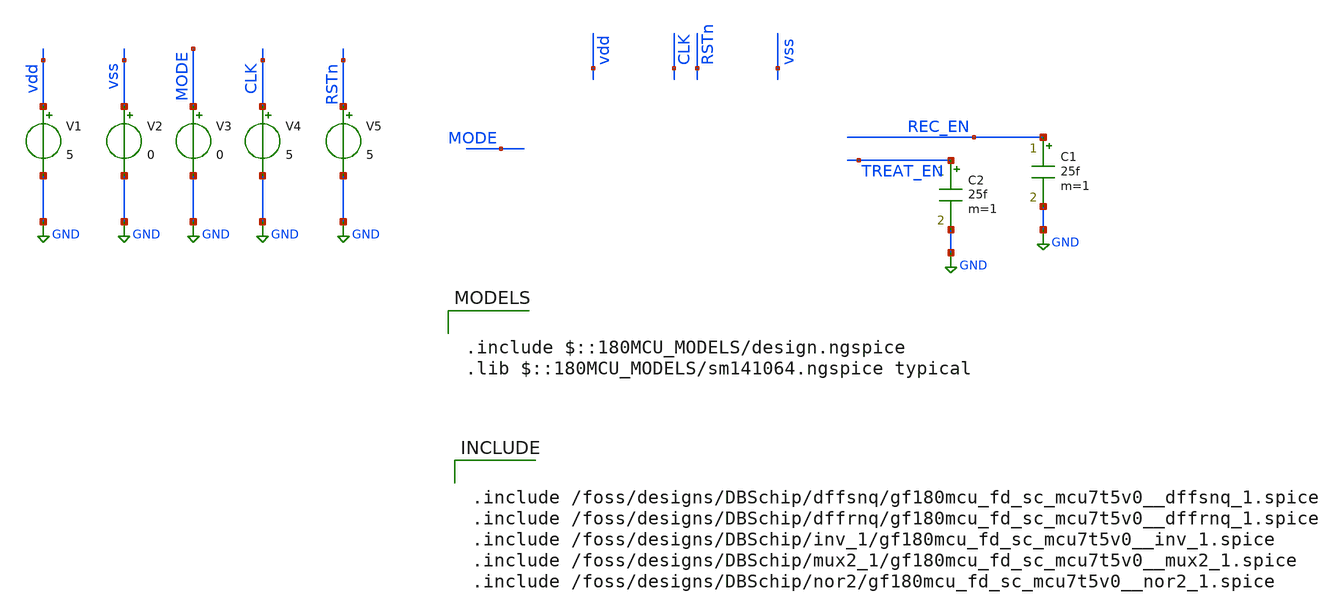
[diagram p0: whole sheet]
** sch_path: FSM/FSM_tb_postPEX.sch
**.subckt FSM_tb_postPEX
V1 vdd GND 5
V2 vss GND 0
V3 MODE GND 0
V4 CLK GND 5
V5 RSTn GND 5
C1 REC_EN GND 25f m=1
C2 TREAT_EN GND 25f m=1
**** begin user architecture code

.include $::180MCU_MODELS/design.ngspice
.lib $::180MCU_MODELS/sm141064.ngspice typical



.include /foss/designs/DBSchip/dffsnq/gf180mcu_fd_sc_mcu7t5v0__dffsnq_1.spice
.include /foss/designs/DBSchip/dffrnq/gf180mcu_fd_sc_mcu7t5v0__dffrnq_1.spice
.include /foss/designs/DBSchip/inv_1/gf180mcu_fd_sc_mcu7t5v0__inv_1.spice
.include /foss/designs/DBSchip/mux2_1/gf180mcu_fd_sc_mcu7t5v0__mux2_1.spice
.include /foss/designs/DBSchip/nor2/gf180mcu_fd_sc_mcu7t5v0__nor2_1.spice




* NGSPICE file created from FSM.ext - technology: gf180mcuD

.subckt dffsnq VNW VPW a_4883_3360# a_4479_2960# a_4470_3360# a_3430_3356# a_3430_2943#
+  a_6267_3356# a_4226_2960# a_6315_3300# a_5411_3360# a_4022_2960# a_4979_3257# a_4539_3312#  a_3902_3312#
+ a_5635_3360# a_3634_2943# a_3222_3356# a_3310_3312# a_7051_2873#
X0 a_7051_2873# a_6315_3300# a_3430_3356# VPW nfet_05v0 ad=0.3586p pd=2.51u as=0.3586p ps=2.51u
+ w=0.815u l=0.6u
X1 a_3634_2943# a_3222_3356# a_3430_3356# VPW nfet_05v0 ad=0.1782p pd=1.69u as=0.1053p ps=0.925u
+ w=0.405u l=0.6u
X2 a_3430_2943# a_3310_3312# a_3222_3356# VNW pfet_05v0 ad=0.2249p pd=1.385u as=0.3806p ps=2.61u
+ w=0.865u l=0.5u
X3 a_3430_3356# a_3310_3312# a_3222_3356# VPW nfet_05v0 ad=0.1053p pd=0.925u as=0.1782p ps=1.69u
+ w=0.405u l=0.6u
X4 a_4022_2960# a_3902_3312# a_3430_3356# VPW nfet_05v0 ad=93.59999f pd=0.88u as=0.1584p ps=1.6u
+ w=0.36u l=0.6u
X5 a_4539_3312# a_4979_3257# a_4883_3360# VPW nfet_05v0 ad=0.1989p pd=1.465u as=86.39999f ps=0.84u
+ w=0.36u l=0.6u
X6 a_5411_3360# a_3634_2943# a_4539_3312# VPW nfet_05v0 ad=93.59999f pd=0.88u as=0.1989p ps=1.465u
+ w=0.36u l=0.6u
X7 a_5635_3360# a_3634_2943# a_5411_3360# VNW pfet_05v0 ad=0.1826p pd=1.71u as=0.1079p ps=0.935u
+ w=0.415u l=0.5u
X8 a_5635_3360# a_4979_3257# a_3430_2943# VNW pfet_05v0 ad=0.2028p pd=1.3u as=0.3432p ps=2.44u
+ w=0.78u l=0.5u
X9 a_3430_3356# a_4539_3312# a_4470_3360# VPW nfet_05v0 ad=93.59999f pd=0.88u as=62.1f ps=0.705u
+ w=0.36u l=0.6u
X10 a_4226_2960# a_3222_3356# a_4022_2960# VPW nfet_05v0 ad=93.59999f pd=0.88u as=93.59999f ps=0.88u
+ w=0.36u l=0.6u
X11 a_3430_2943# a_4979_3257# a_4539_3312# VNW pfet_05v0 ad=0.4149p pd=2.65u as=0.1521p ps=1.105u
+ w=0.585u l=0.5u
X12 a_4883_3360# a_4226_2960# a_3430_3356# VPW nfet_05v0 ad=86.39999f pd=0.84u as=93.59999f ps=0.88u
+ w=0.36u l=0.6u
X13 a_6315_3300# a_5411_3360# a_3430_2943# VNW pfet_05v0 ad=0.3432p pd=2.44u as=0.3276p ps=1.62u
+ w=0.78u l=0.5u
X14 a_4470_3360# a_3634_2943# a_4226_2960# VPW nfet_05v0 ad=62.1f pd=0.705u as=93.59999f ps=0.88u
+ w=0.36u l=0.6u
X15 a_6315_3300# a_5411_3360# a_3430_3356# VPW nfet_05v0 ad=0.1782p pd=1.69u as=0.14985p ps=1.145u
+ w=0.405u l=0.6u
X16 a_3634_2943# a_3222_3356# a_3430_2943# VNW pfet_05v0 ad=0.3806p pd=2.61u as=0.2249p ps=1.385u
+ w=0.865u l=0.5u
X17 a_5411_3360# a_3222_3356# a_4539_3312# VNW pfet_05v0 ad=0.1079p pd=0.935u as=0.27805p ps=2.17u
+ w=0.415u l=0.5u
X18 a_3430_3356# a_6315_3300# a_6267_3356# VPW nfet_05v0 ad=0.14985p pd=1.145u as=48.6f ps=0.645u
+ w=0.405u l=0.6u
X19 a_4226_2960# a_3634_2943# a_4022_2960# VNW pfet_05v0 ad=0.19315p pd=1.27u as=0.1313p ps=1.025u
+ w=0.505u l=0.5u
X20 a_4539_3312# a_4226_2960# a_3430_2943# VNW pfet_05v0 ad=0.1521p pd=1.105u as=0.3975p ps=2.185u
+ w=0.585u l=0.5u
X21 a_6267_3356# a_4979_3257# a_5635_3360# VPW nfet_05v0 ad=48.6f pd=0.645u as=0.3123p ps=2.38u
+ w=0.405u l=0.6u
X22 a_4022_2960# a_3902_3312# a_3430_2943# VNW pfet_05v0 ad=0.1313p pd=1.025u as=0.22725p ps=1.91u
+ w=0.505u l=0.5u
X23 a_3430_2943# a_6315_3300# a_5635_3360# VNW pfet_05v0 ad=0.3276p pd=1.62u as=0.2028p ps=1.3u
+ w=0.78u l=0.5u
X24 a_4479_2960# a_3222_3356# a_4226_2960# VNW pfet_05v0 ad=0.101p pd=0.905u as=0.19315p ps=1.27u
+ w=0.505u l=0.5u
X25 a_5635_3360# a_3222_3356# a_5411_3360# VPW nfet_05v0 ad=0.2898p pd=2.33u as=93.59999f ps=0.88u
+ w=0.36u l=0.6u
X26 a_7051_2873# a_6315_3300# a_3430_2943# VNW pfet_05v0 ad=0.6561p pd=3.51u as=0.5346p ps=3.31u
+ w=1.215u l=0.5u
X27 a_3430_2943# a_4539_3312# a_4479_2960# VNW pfet_05v0 ad=0.3975p pd=2.185u as=0.101p ps=0.905u
+ w=0.505u l=0.5u
C0 a_4979_3257# a_3222_3356# 0.07762f
C1 a_5411_3360# a_6267_3356# 0.00413f
C2 a_5411_3360# a_3430_2943# 0.07341f
C3 a_4226_2960# a_4479_2960# 0.00215f
C4 a_4226_2960# a_4539_3312# 0.38667f
C5 VNW a_3310_3312# 0.13342f
C6 a_3430_2943# a_3902_3312# 0.00494f
C7 VNW a_3430_3356# 0.00946f
C8 a_4979_3257# a_4539_3312# 0.07298f
C9 a_4226_2960# a_4470_3360# 0
C10 a_3430_2943# a_7051_2873# 0.28218f
C11 a_5411_3360# a_6315_3300# 0.51404f
C12 a_3430_2943# a_6267_3356# 0
C13 a_3634_2943# a_3310_3312# 0.00131f
C14 a_5411_3360# a_4979_3257# 0.0706f
C15 a_3634_2943# a_3430_3356# 1.08287f
C16 a_4226_2960# a_3902_3312# 0
C17 a_3222_3356# a_3310_3312# 0.70196f
C18 a_3222_3356# a_3430_3356# 0.29459f
C19 a_7051_2873# a_6315_3300# 0.17947f
C20 a_5635_3360# VNW 0.04382f
C21 a_4022_2960# a_3430_3356# 0.05001f
C22 a_3430_2943# a_6315_3300# 0.35131f
C23 a_4539_3312# a_3430_3356# 0.02825f
C24 a_3634_2943# VNW 0.40096f
C25 a_3430_2943# a_4226_2960# 0.03968f
C26 VNW a_3222_3356# 0.90809f
C27 a_5635_3360# a_3634_2943# 0.05668f
C28 a_4979_3257# a_3430_2943# 0.12782f
C29 a_4470_3360# a_3430_3356# 0.00364f
C30 a_4022_2960# VNW 0.01368f
C31 a_5635_3360# a_3222_3356# 0.00597f
C32 a_5411_3360# a_3430_3356# 1.19047f
C33 VNW a_4539_3312# 0.21951f
C34 a_3634_2943# a_3222_3356# 0.47313f
C35 a_5635_3360# a_4539_3312# 0
C36 a_4022_2960# a_3634_2943# 0.42776f
C37 a_3902_3312# a_3430_3356# 0.06788f
C38 a_4979_3257# a_6315_3300# 0.08929f
C39 a_4979_3257# a_4226_2960# 0.06324f
C40 a_4022_2960# a_3222_3356# 0.0157f
C41 a_7051_2873# a_3430_3356# 0.13127f
C42 a_5411_3360# VNW 0.20903f
C43 a_3634_2943# a_4539_3312# 0.31725f
C44 a_3222_3356# a_4479_2960# 0.00838f
C45 a_5411_3360# a_5635_3360# 0.56917f
C46 a_4539_3312# a_3222_3356# 0.84088f
C47 a_3430_2943# a_3310_3312# 0.02223f
C48 a_3430_2943# a_3430_3356# 0.01381f
C49 a_3634_2943# a_4470_3360# 0.00269f
C50 VNW a_3902_3312# 0.16142f
C51 VNW a_7051_2873# 0.03162f
C52 a_4883_3360# a_3634_2943# 0.00762f
C53 a_4539_3312# a_4479_2960# 0
C54 a_5411_3360# a_3634_2943# 0.154f
C55 a_5411_3360# a_3222_3356# 0.15368f
C56 a_3430_3356# a_6315_3300# 0.13908f
C57 a_3430_2943# VNW 0.53642f
C58 a_3634_2943# a_3902_3312# 0.4001f
C59 a_4226_2960# a_3430_3356# 0.06133f
C60 a_5635_3360# a_6267_3356# 0.0012f
C61 a_3430_2943# a_5635_3360# 0.20863f
C62 a_3902_3312# a_3222_3356# 0.0927f
C63 a_3634_2943# a_7051_2873# 0
C64 a_4883_3360# a_4539_3312# 0.00275f
C65 a_4022_2960# a_3902_3312# 0.1081f
C66 a_4979_3257# a_3430_3356# 0.01045f
C67 a_7051_2873# a_3222_3356# 0
C68 a_5411_3360# a_4539_3312# 0.15287f
C69 a_3430_2943# a_3634_2943# 0.62458f
C70 VNW a_6315_3300# 0.32346f
C71 a_4226_2960# VNW 0.22464f
C72 a_3430_2943# a_3222_3356# 1.41458f
C73 a_5635_3360# a_6315_3300# 0.00955f
C74 a_4979_3257# VNW 0.81105f
C75 a_4979_3257# a_5635_3360# 0.30222f
C76 a_3430_2943# a_4539_3312# 0.01626f
C77 a_3634_2943# a_6315_3300# 0
C78 a_4226_2960# a_3634_2943# 0.86961f
C79 a_5411_3360# a_7051_2873# 0
C80 a_3222_3356# a_6315_3300# 0
C81 a_4226_2960# a_3222_3356# 0.20702f
C82 a_3310_3312# a_3430_3356# 0.02287f
C83 a_4979_3257# a_3634_2943# 0.0839f
C84 a_4226_2960# a_4022_2960# 0.06821f
C85 VNW VPW 6.37108f
C86 a_7051_2873# VPW 0.10557f
C87 a_6315_3300# VPW 0.58406f
C88 a_5635_3360# VPW 0.04999f
C89 a_5411_3360# VPW 0.43408f
C90 a_3430_2943# VPW 0.83584f
C91 a_4022_2960# VPW 0.01977f
C92 a_4979_3257# VPW 0.71025f
C93 a_4226_2960# VPW 0.30208f
C94 a_4539_3312# VPW 0.28651f
C95 a_3902_3312# VPW 0.24718f
C96 a_3634_2943# VPW 1.21246f
C97 a_3430_3356# VPW 1.53117f
C98 a_3310_3312# VPW 0.2938f
C99 a_3222_3356# VPW 1.31514f
.ends

.subckt mux21 VNW VPW a_n2035_3346# a_n2339_2762# a_n2427_3346# a_n2807_3163# a_n2394_2806#
+  a_n1987_2762# a_n2687_2806# a_n2687_3290# a_n2035_2806# a_n2547_3163# a_n2379_3163#  a_n2895_3290#
X0 a_n2035_2806# a_n2379_3163# a_n2807_3163# VNW pfet_05v0 ad=73.8f pd=0.855u as=0.1599p ps=1.135u
+ w=0.615u l=0.5u
X1 a_n2687_2806# a_n1987_2762# a_n2035_2806# VNW pfet_05v0 ad=0.1599p pd=1.135u as=73.8f ps=0.855u
+ w=0.615u l=0.5u
X2 a_n2687_3290# a_n1987_2762# a_n2035_3346# VPW nfet_05v0 ad=93.59999f pd=0.88u as=43.2f ps=0.6u
+ w=0.36u l=0.6u
X3 a_n2427_3346# a_n2547_3163# a_n2687_3290# VPW nfet_05v0 ad=43.2f pd=0.6u as=0.218p ps=1.52u
+ w=0.36u l=0.6u
X4 a_n2339_2762# a_n2379_3163# a_n2687_3290# VPW nfet_05v0 ad=0.1584p pd=1.6u as=93.59999f ps=0.88u
+ w=0.36u l=0.6u
X5 a_n2807_3163# a_n2339_2762# a_n2394_2806# VNW pfet_05v0 ad=0.1599p pd=1.135u as=84.55f ps=0.89u
+ w=0.615u l=0.5u
X6 a_n2687_2806# a_n2807_3163# a_n2895_3290# VNW pfet_05v0 ad=0.42982p pd=2.185u as=0.5368p ps=3.32u
+ w=1.22u l=0.5u
X7 a_n2807_3163# a_n2379_3163# a_n2427_3346# VPW nfet_05v0 ad=93.59999f pd=0.88u as=43.2f ps=0.6u
+ w=0.36u l=0.6u
X8 a_n2035_3346# a_n2339_2762# a_n2807_3163# VPW nfet_05v0 ad=43.2f pd=0.6u as=93.59999f ps=0.88u
+ w=0.36u l=0.6u
X9 a_n2339_2762# a_n2379_3163# a_n2687_2806# VNW pfet_05v0 ad=0.2706p pd=2.11u as=0.1599p ps=1.135u
+ w=0.615u l=0.5u
X10 a_n2687_3290# a_n2807_3163# a_n2895_3290# VPW nfet_05v0 ad=0.218p pd=1.52u as=0.3608p ps=2.52u
+ w=0.82u l=0.6u
X11 a_n2394_2806# a_n2547_3163# a_n2687_2806# VNW pfet_05v0 ad=84.55f pd=0.89u as=0.42982p ps=2.185u
+ w=0.615u l=0.5u
C0 a_n2379_3163# a_n2394_2806# 0
C1 a_n2339_2762# a_n1987_2762# 0.44871f
C2 a_n2339_2762# a_n2807_3163# 0.03132f
C3 a_n2547_3163# a_n2687_3290# 0.01931f
C4 a_n1987_2762# a_n2687_2806# 0.02643f
C5 VNW a_n2379_3163# 0.35854f
C6 a_n2807_3163# a_n2687_2806# 0.57837f
C7 a_n2547_3163# a_n2895_3290# 0.00111f
C8 a_n2807_3163# a_n1987_2762# 0.00457f
C9 a_n2547_3163# a_n2394_2806# 0
C10 a_n2339_2762# a_n2379_3163# 0.31909f
C11 a_n2035_2806# a_n2339_2762# 0
C12 a_n2687_3290# a_n2895_3290# 0.07969f
C13 a_n2687_2806# a_n2379_3163# 0.20342f
C14 a_n2035_2806# a_n2687_2806# 0.00486f
C15 a_n2547_3163# VNW 0.19864f
C16 a_n2035_3346# a_n2687_3290# 0.0022f
C17 a_n1987_2762# a_n2379_3163# 0.61564f
C18 a_n2687_3290# VNW 0.00651f
C19 a_n2807_3163# a_n2379_3163# 0.22045f
C20 a_n2035_2806# a_n2807_3163# 0.00106f
C21 a_n2339_2762# a_n2547_3163# 0.06637f
C22 a_n2807_3163# a_n2427_3346# 0.00317f
C23 a_n2687_2806# a_n2547_3163# 0.01544f
C24 VNW a_n2895_3290# 0.03019f
C25 a_n2339_2762# a_n2687_3290# 0.30506f
C26 a_n2687_2806# a_n2687_3290# 0.01065f
C27 a_n1987_2762# a_n2547_3163# 0
C28 a_n2035_2806# a_n2379_3163# 0.00276f
C29 a_n2807_3163# a_n2547_3163# 0.45783f
C30 a_n1987_2762# a_n2687_3290# 0.03158f
C31 a_n2339_2762# a_n2394_2806# 0
C32 a_n2807_3163# a_n2687_3290# 0.53787f
C33 a_n2687_2806# a_n2895_3290# 0.09438f
C34 a_n2035_3346# a_n2339_2762# 0.00166f
C35 a_n2687_2806# a_n2394_2806# 0.0019f
C36 a_n2339_2762# VNW 0.27449f
C37 a_n2547_3163# a_n2379_3163# 0.3671f
C38 a_n2807_3163# a_n2895_3290# 0.13298f
C39 a_n2687_2806# VNW 0.16121f
C40 a_n2807_3163# a_n2394_2806# 0.00556f
C41 a_n2427_3346# a_n2547_3163# 0
C42 a_n2035_3346# a_n2807_3163# 0.00101f
C43 a_n2687_3290# a_n2379_3163# 0.04663f
C44 a_n1987_2762# VNW 0.18121f
C45 a_n2427_3346# a_n2687_3290# 0
C46 a_n2807_3163# VNW 0.16283f
C47 a_n2339_2762# a_n2687_2806# 0.14217f
C48 VNW VPW 2.50194f
C49 a_n2687_2806# VPW 0.34621f
C50 a_n1987_2762# VPW 0.29252f
C51 a_n2339_2762# VPW 0.4399f
C52 a_n2379_3163# VPW 0.64969f
C53 a_n2547_3163# VPW 0.31807f
C54 a_n2687_3290# VPW 0.57909f
C55 a_n2895_3290# VPW 0.11309f
C56 a_n2807_3163# VPW 0.3249f
.ends

.subckt dffrnq VNW VPW a_1667_2471# a_563_2471# a_311_2787# a_395_2471# a_n649_2466#  a_2776_2384#
+ a_1772_2427# a_1355_2471# a_n649_2787# a_2148_2471# a_611_2339# a_n857_2466#  a_n197_2617# a_n445_2787#
+ a_415_2738# a_107_2787# a_n97_2787# a_n769_2422#
X0 a_n649_2787# a_n769_2422# a_n857_2466# VNW pfet_05v0 ad=0.2249p pd=1.385u as=0.3806p ps=2.61u
+ w=0.865u l=0.5u
X1 a_311_2787# a_n857_2466# a_107_2787# VNW pfet_05v0 ad=0.2028p pd=1.3u as=0.2028p ps=1.3u w=0.78u
+ l=0.5u
X2 a_2148_2471# a_611_2339# a_n649_2466# VPW nfet_05v0 ad=0.134p pd=1.1u as=0.1224p ps=1.04u w=0.36u
+ l=0.6u
X3 a_1355_2471# a_n445_2787# a_415_2738# VPW nfet_05v0 ad=0.2007p pd=1.475u as=0.2007p ps=1.475u
+ w=0.36u l=0.6u
X4 a_107_2787# a_n857_2466# a_n97_2787# VPW nfet_05v0 ad=93.59999f pd=0.88u as=93.59999f ps=0.88u
+ w=0.36u l=0.6u
X5 a_311_2787# a_611_2339# a_n649_2787# VNW pfet_05v0 ad=0.3432p pd=2.44u as=0.45p ps=2.02u w=0.78u
+ l=0.5u
X6 a_n649_2466# a_611_2339# a_563_2471# VPW nfet_05v0 ad=0.2016p pd=1.48u as=43.2f ps=0.6u w=0.36u
+ l=0.6u
X7 a_2776_2384# a_1772_2427# a_n649_2466# VPW nfet_05v0 ad=0.3586p pd=2.51u as=0.3586p ps=2.51u
+ w=0.815u l=0.6u
X8 a_n649_2787# a_1772_2427# a_1667_2471# VNW pfet_05v0 ad=0.29465p pd=1.74u as=0.1313p ps=1.025u
+ w=0.505u l=0.5u
X9 a_107_2787# a_n445_2787# a_n97_2787# VNW pfet_05v0 ad=0.2028p pd=1.3u as=0.2028p ps=1.3u w=0.78u
+ l=0.5u
X10 a_n97_2787# a_n197_2617# a_n649_2466# VPW nfet_05v0 ad=93.59999f pd=0.88u as=0.1584p ps=1.6u
+ w=0.36u l=0.6u
X11 a_563_2471# a_415_2738# a_395_2471# VPW nfet_05v0 ad=43.2f pd=0.6u as=43.2f ps=0.6u w=0.36u
+ l=0.6u
X12 a_n649_2787# a_1355_2471# a_1772_2427# VNW pfet_05v0 ad=0.44p pd=2.88u as=0.26p ps=1.52u w=1u
+ l=0.5u
X13 a_395_2471# a_n445_2787# a_107_2787# VPW nfet_05v0 ad=43.2f pd=0.6u as=93.59999f ps=0.88u
+ w=0.36u l=0.6u
X14 a_415_2738# a_107_2787# a_n649_2787# VNW pfet_05v0 ad=0.2424p pd=1.465u as=0.2222p ps=1.89u
+ w=0.505u l=0.5u
X15 a_2776_2384# a_1772_2427# a_n649_2787# VNW pfet_05v0 ad=0.5346p pd=3.31u as=0.5346p ps=3.31u
+ w=1.215u l=0.5u
X16 a_n649_2466# a_1772_2427# a_1667_2471# VPW nfet_05v0 ad=0.1224p pd=1.04u as=94.5f ps=0.885u
+ w=0.36u l=0.6u
X17 a_n97_2787# a_n197_2617# a_n649_2787# VNW pfet_05v0 ad=0.2028p pd=1.3u as=0.3432p ps=2.44u
+ w=0.78u l=0.5u
X18 a_n445_2787# a_n857_2466# a_n649_2787# VNW pfet_05v0 ad=0.3806p pd=2.61u as=0.2249p ps=1.385u
+ w=0.865u l=0.5u
X19 a_n649_2787# a_415_2738# a_311_2787# VNW pfet_05v0 ad=0.45p pd=2.02u as=0.2028p ps=1.3u w=0.78u
+ l=0.5u
X20 a_n649_2466# a_n769_2422# a_n857_2466# VPW nfet_05v0 ad=0.1053p pd=0.925u as=0.1782p ps=1.69u
+ w=0.405u l=0.6u
X21 a_1667_2471# a_n857_2466# a_1355_2471# VPW nfet_05v0 ad=94.5f pd=0.885u as=0.2007p ps=1.475u
+ w=0.36u l=0.6u
X22 a_415_2738# a_107_2787# a_n649_2466# VPW nfet_05v0 ad=0.2007p pd=1.475u as=0.2016p ps=1.48u
+ w=0.36u l=0.6u
X23 a_n445_2787# a_n857_2466# a_n649_2466# VPW nfet_05v0 ad=0.1782p pd=1.69u as=0.1053p ps=0.925u
+ w=0.405u l=0.6u
X24 a_1355_2471# a_n857_2466# a_415_2738# VNW pfet_05v0 ad=0.25375p pd=1.51u as=0.2424p ps=1.465u
+ w=0.505u l=0.5u
X25 a_1772_2427# a_1355_2471# a_2148_2471# VPW nfet_05v0 ad=0.176p pd=1.68u as=0.134p ps=1.1u w=0.4u
+ l=0.6u
X26 a_1667_2471# a_n445_2787# a_1355_2471# VNW pfet_05v0 ad=0.1313p pd=1.025u as=0.25375p ps=1.51u
+ w=0.505u l=0.5u
X27 a_1772_2427# a_611_2339# a_n649_2787# VNW pfet_05v0 ad=0.26p pd=1.52u as=0.29465p ps=1.74u w=1u
+ l=0.5u
C0 a_311_2787# a_n445_2787# 0.009f
C1 a_n197_2617# a_n445_2787# 0.32879f
C2 a_611_2339# a_n649_2787# 0.03498f
C3 a_n649_2787# a_1355_2471# 1.11667f
C4 VNW a_n649_2787# 0.50089f
C5 a_n649_2466# a_n649_2787# 0.01338f
C6 a_n857_2466# a_n445_2787# 0.53697f
C7 a_107_2787# a_n649_2787# 0.11921f
C8 a_n769_2422# a_n857_2466# 0.6696f
C9 a_611_2339# a_1355_2471# 0.09434f
C10 a_n197_2617# a_n97_2787# 0.08286f
C11 VNW a_611_2339# 0.32949f
C12 VNW a_1355_2471# 0.21243f
C13 a_n649_2466# a_611_2339# 0.44197f
C14 a_n649_2466# a_1355_2471# 0.03047f
C15 a_611_2339# a_107_2787# 0.0832f
C16 a_107_2787# a_1355_2471# 0.00123f
C17 VNW a_n649_2466# 0.0106f
C18 a_1772_2427# a_n857_2466# 0.01904f
C19 VNW a_107_2787# 0.24136f
C20 a_n649_2466# a_107_2787# 0.04356f
C21 a_1667_2471# a_n857_2466# 0.00367f
C22 a_n857_2466# a_n97_2787# 0.01185f
C23 a_n857_2466# a_2776_2384# 0
C24 a_n649_2466# a_563_2471# 0.0019f
C25 a_107_2787# a_563_2471# 0
C26 a_415_2738# a_n445_2787# 0.8821f
C27 a_n649_2466# a_395_2471# 0.0017f
C28 a_107_2787# a_395_2471# 0
C29 a_n649_2787# a_311_2787# 0.28263f
C30 a_n197_2617# a_n649_2787# 0.00937f
C31 a_611_2339# a_311_2787# 0.02104f
C32 a_n857_2466# a_n649_2787# 0.41709f
C33 VNW a_311_2787# 0.01627f
C34 VNW a_n197_2617# 0.12821f
C35 a_2148_2471# a_1772_2427# 0.00177f
C36 a_n649_2466# a_n197_2617# 0.06462f
C37 a_107_2787# a_311_2787# 0.66083f
C38 a_n197_2617# a_107_2787# 0
C39 a_611_2339# a_n857_2466# 0.0801f
C40 a_n857_2466# a_1355_2471# 0.0428f
C41 VNW a_n857_2466# 1.28735f
C42 a_n649_2466# a_n857_2466# 0.29126f
C43 a_107_2787# a_n857_2466# 0.08126f
C44 a_n769_2422# a_n445_2787# 0.00276f
C45 a_1772_2427# a_n445_2787# 0.02046f
C46 a_1667_2471# a_n445_2787# 0.27749f
C47 a_n97_2787# a_n445_2787# 0.40164f
C48 a_415_2738# a_n649_2787# 0.09419f
C49 a_1667_2471# a_1772_2427# 0.11606f
C50 a_415_2738# a_611_2339# 0.07929f
C51 a_415_2738# a_1355_2471# 0.05672f
C52 a_611_2339# a_2148_2471# 0.01068f
C53 VNW a_415_2738# 0.14901f
C54 a_1772_2427# a_2776_2384# 0.10944f
C55 a_n649_2466# a_415_2738# 0.01387f
C56 a_415_2738# a_107_2787# 0.93419f
C57 a_n857_2466# a_311_2787# 0.007f
C58 a_n197_2617# a_n857_2466# 0.09411f
C59 a_n649_2787# a_n445_2787# 0.45627f
C60 a_n769_2422# a_n649_2787# 0.02303f
C61 a_611_2339# a_n445_2787# 0.07873f
C62 a_n445_2787# a_1355_2471# 0.51037f
C63 VNW a_n445_2787# 0.34128f
C64 a_1772_2427# a_n649_2787# 0.10205f
C65 a_n649_2466# a_n445_2787# 1.20207f
C66 a_107_2787# a_n445_2787# 0.36196f
C67 a_1667_2471# a_n649_2787# 0.00217f
C68 a_n769_2422# VNW 0.1337f
C69 a_n649_2787# a_n97_2787# 0
C70 a_n769_2422# a_n649_2466# 0.02195f
C71 a_n649_2787# a_2776_2384# 0.14934f
C72 a_611_2339# a_1772_2427# 0.33647f
C73 a_1772_2427# a_1355_2471# 0.63332f
C74 a_415_2738# a_311_2787# 0.02667f
C75 a_563_2471# a_n445_2787# 0.00227f
C76 VNW a_1772_2427# 0.35472f
C77 a_1667_2471# a_611_2339# 0.03878f
C78 a_n649_2466# a_1772_2427# 0.185f
C79 a_1667_2471# a_1355_2471# 0.11969f
C80 VNW a_1667_2471# 0.02016f
C81 VNW a_n97_2787# 0.01023f
C82 a_n649_2466# a_1667_2471# 0.1285f
C83 a_611_2339# a_2776_2384# 0
C84 a_n649_2466# a_n97_2787# 0.05215f
C85 a_2776_2384# a_1355_2471# 0.01436f
C86 a_107_2787# a_n97_2787# 0.04844f
C87 VNW a_2776_2384# 0.03444f
C88 a_n649_2466# a_2776_2384# 0.1134f
C89 a_415_2738# a_n857_2466# 0.05539f
C90 a_395_2471# a_n445_2787# 0.00207f
C91 VNW VPW 6.06621f
C92 a_2776_2384# VPW 0.11476f
C93 a_n649_2466# VPW 1.26186f
C94 a_1667_2471# VPW 0.01697f
C95 a_1772_2427# VPW 0.62251f
C96 a_1355_2471# VPW 0.37166f
C97 a_611_2339# VPW 1.36673f
C98 a_311_2787# VPW 0.01297f
C99 a_107_2787# VPW 0.29173f
C100 a_n97_2787# VPW 0.02321f
C101 a_415_2738# VPW 0.27904f
C102 a_n197_2617# VPW 0.25343f
C103 a_n445_2787# VPW 0.68441f
C104 a_n649_2787# VPW 0.80211f
C105 a_n769_2422# VPW 0.29458f
C106 a_n857_2466# VPW 1.43686f
.ends

.subckt nor2_1 a_n5117_4170# a_n4805_3759# a_n5029_3759# a_n5117_3803# a_n4909_3803#  a_n4929_4170#
+ w_n5239_4050# VSUBS
X0 a_n5117_3803# a_n4805_3759# a_n4909_3803# VSUBS nfet_05v0 ad=0.2486p pd=2.01u as=0.1469p
+ ps=1.085u w=0.565u l=0.6u
X1 a_n4929_4170# a_n5029_3759# a_n5117_4170# w_n5239_4050# pfet_05v0 ad=0.4087p pd=1.89u as=0.5368p
+ ps=3.32u w=1.22u l=0.5u
X2 a_n4909_3803# a_n5029_3759# a_n5117_3803# VSUBS nfet_05v0 ad=0.1469p pd=1.085u as=0.2486p
+ ps=2.01u w=0.565u l=0.6u
X3 a_n4909_3803# a_n4805_3759# a_n4929_4170# w_n5239_4050# pfet_05v0 ad=0.5368p pd=3.32u as=0.4087p
+ ps=1.89u w=1.22u l=0.5u
C0 a_n5029_3759# a_n4805_3759# 0.03781f
C1 a_n5117_3803# w_n5239_4050# 0.01397f
C2 w_n5239_4050# a_n4805_3759# 0.12879f
C3 a_n4909_3803# a_n5029_3759# 0.37841f
C4 a_n4909_3803# w_n5239_4050# 0.0217f
C5 a_n5029_3759# w_n5239_4050# 0.1288f
C6 a_n4929_4170# a_n5117_4170# 0.01396f
C7 a_n5117_3803# a_n5117_4170# 0.02578f
C8 a_n5117_4170# a_n4805_3759# 0.02269f
C9 a_n4929_4170# a_n5117_3803# 0
C10 a_n4909_3803# a_n5117_4170# 0.11792f
C11 a_n5117_3803# a_n4805_3759# 0.13941f
C12 a_n5117_4170# a_n5029_3759# 0.25532f
C13 a_n5117_4170# w_n5239_4050# 0.09389f
C14 a_n4909_3803# a_n4929_4170# 0.02369f
C15 a_n4909_3803# a_n5117_3803# 0.10123f
C16 a_n4909_3803# a_n4805_3759# 0.46284f
C17 a_n4929_4170# a_n5029_3759# 0.00898f
C18 a_n5117_3803# a_n5029_3759# 0.04335f
C19 a_n5117_3803# VSUBS 0.33074f
C20 a_n4909_3803# VSUBS 0.06183f
C21 a_n5117_4170# VSUBS 0.21851f
C22 a_n4805_3759# VSUBS 0.32338f
C23 a_n5029_3759# VSUBS 0.33451f
C24 w_n5239_4050# VSUBS 1.31158f
.ends

.subckt nor2_2 a_n3913_1897# a_n3601_1486# a_n3705_1530# a_n3725_1897# a_n3825_1486#  w_n4035_1777#
+ a_n3913_1530# VSUBS
X0 a_n3725_1897# a_n3825_1486# a_n3913_1897# w_n4035_1777# pfet_05v0 ad=0.4087p pd=1.89u as=0.5368p
+ ps=3.32u w=1.22u l=0.5u
X1 a_n3705_1530# a_n3825_1486# a_n3913_1530# VSUBS nfet_05v0 ad=0.1469p pd=1.085u as=0.2486p
+ ps=2.01u w=0.565u l=0.6u
X2 a_n3913_1530# a_n3601_1486# a_n3705_1530# VSUBS nfet_05v0 ad=0.2486p pd=2.01u as=0.1469p
+ ps=1.085u w=0.565u l=0.6u
X3 a_n3705_1530# a_n3601_1486# a_n3725_1897# w_n4035_1777# pfet_05v0 ad=0.5368p pd=3.32u as=0.4087p
+ ps=1.89u w=1.22u l=0.5u
C0 a_n3705_1530# a_n3601_1486# 0.57973f
C1 w_n4035_1777# a_n3705_1530# 0.01867f
C2 a_n3725_1897# a_n3825_1486# 0.00898f
C3 a_n3913_1530# a_n3705_1530# 0.08687f
C4 a_n3913_1897# a_n3705_1530# 0.11792f
C5 a_n3825_1486# a_n3705_1530# 0.37841f
C6 a_n3725_1897# a_n3705_1530# 0.02369f
C7 w_n4035_1777# a_n3601_1486# 0.13462f
C8 a_n3913_1530# a_n3601_1486# 0.16863f
C9 a_n3913_1897# a_n3601_1486# 0.02804f
C10 w_n4035_1777# a_n3913_1530# 0.01057f
C11 w_n4035_1777# a_n3913_1897# 0.09154f
C12 a_n3913_1530# a_n3913_1897# 0.02322f
C13 a_n3825_1486# a_n3601_1486# 0.03781f
C14 w_n4035_1777# a_n3825_1486# 0.1288f
C15 a_n3913_1530# a_n3825_1486# 0.04335f
C16 a_n3825_1486# a_n3913_1897# 0.25532f
C17 a_n3913_1530# a_n3725_1897# 0
C18 a_n3725_1897# a_n3913_1897# 0.01396f
C19 a_n3913_1530# VSUBS 0.33149f
C20 a_n3705_1530# VSUBS 0.06f
C21 a_n3913_1897# VSUBS 0.22019f
C22 a_n3601_1486# VSUBS 0.33415f
C23 a_n3825_1486# VSUBS 0.33451f
C24 w_n4035_1777# VSUBS 1.24009f
.ends

.subckt inv1 VNW VPW a_142_558# a_210_110# a_122_154# a_330_154#
X0 a_330_154# a_210_110# a_122_154# VPW nfet_05v0 ad=0.3608p pd=2.52u as=0.3608p ps=2.52u w=0.82u
+ l=0.6u
X1 a_330_154# a_210_110# a_142_558# VNW pfet_05v0 ad=0.5368p pd=3.32u as=0.5368p ps=3.32u w=1.22u
+ l=0.5u
C0 a_122_154# a_210_110# 0.0533f
C1 VNW a_142_558# 0.07626f
C2 a_330_154# a_142_558# 0.13738f
C3 VNW a_330_154# 0.0222f
C4 a_210_110# a_142_558# 0.04185f
C5 a_122_154# a_142_558# 0.02563f
C6 VNW a_210_110# 0.13776f
C7 a_210_110# a_330_154# 0.2622f
C8 VNW a_122_154# 0.01134f
C9 a_122_154# a_330_154# 0.1153f
C10 VNW VPW 0.96348f
C11 a_122_154# VPW 0.2316f
C12 a_330_154# VPW 0.1134f
C13 a_142_558# VPW 0.18114f
C14 a_210_110# VPW 0.34198f
.ends

.subckt FSM MODE RSTn VSS CLK VDD TREAT_EN REC_EN
Xdffsnq_0 VDD VSS dffsnq_0/a_4883_3360# dffsnq_0/a_4479_2960# dffsnq_0/a_4470_3360#  VSS VDD
+ dffsnq_0/a_6267_3356# dffsnq_0/a_4226_2960# dffsnq_0/a_6315_3300# dffsnq_0/a_5411_3360#  dffsnq_0/a_4022_2960# RSTn
+ dffsnq_0/a_4539_3312# m2_n1268_1517# dffsnq_0/a_5635_3360#  dffsnq_0/a_3634_2943# dffsnq_0/a_3222_3356# CLK
+ m2_n2888_1381# dffsnq
Xmux21_0 VDD VSS mux21_0/a_n2035_3346# mux21_0/a_n2339_2762# mux21_0/a_n2427_3346#
+  mux21_0/a_n2807_3163# mux21_0/a_n2394_2806# REC_EN VDD VSS mux21_0/a_n2035_2806#  TREAT_EN MODE m2_n1268_1517# mux21
Xdffrnq_0 VDD VSS dffrnq_0/a_1667_2471# dffrnq_0/a_563_2471# dffrnq_0/a_311_2787#
+  dffrnq_0/a_395_2471# VSS REC_EN dffrnq_0/a_1772_2427# dffrnq_0/a_1355_2471# VDD  dffrnq_0/a_2148_2471# RSTn
+ dffrnq_0/a_n857_2466# m2_n1118_2715# dffrnq_0/a_n445_2787#  dffrnq_0/a_415_2738# dffrnq_0/a_107_2787#
+ dffrnq_0/a_n97_2787# CLK dffrnq
Xnor2_1_0 VDD REC_EN m2_n2888_1381# VSS TREAT_EN nor2_1_0/a_n4929_4170# VDD VSS nor2_1
Xnor2_2_0 VDD TREAT_EN m2_n1118_2715# nor2_2_0/a_n3725_1897# m1_n1940_2465# VDD VSS  VSS nor2_2
Xinv1_0 VDD VSS VDD MODE VSS m1_n1940_2465# inv1
C0 mux21_0/a_n2035_3346# MODE 0
C1 dffsnq_0/a_3222_3356# dffrnq_0/a_n445_2787# 0
C2 RSTn dffrnq_0/a_415_2738# 0
C3 CLK m2_n1118_2715# 0.15521f
C4 dffrnq_0/a_2148_2471# m2_n2888_1381# 0
C5 VDD dffsnq_0/a_5411_3360# 0.00119f
C6 dffsnq_0/a_5635_3360# dffsnq_0/a_5411_3360# -0
C7 TREAT_EN dffrnq_0/a_n857_2466# 0.0154f
C8 REC_EN dffsnq_0/a_4479_2960# 0
C9 m1_n1940_2465# dffrnq_0/a_n857_2466# 0
C10 dffrnq_0/a_395_2471# REC_EN 0
C11 REC_EN RSTn 0.04521f
C12 dffsnq_0/a_4226_2960# VDD 0
C13 REC_EN dffrnq_0/a_415_2738# 0.03883f
C14 mux21_0/a_n2427_3346# MODE 0
C15 dffsnq_0/a_4539_3312# CLK 0
C16 dffsnq_0/a_4470_3360# CLK 0
C17 mux21_0/a_n2035_2806# m2_n2888_1381# 0.0019f
C18 dffsnq_0/a_3634_2943# dffrnq_0/a_n445_2787# 0
C19 VDD dffrnq_0/a_n97_2787# -0
C20 dffrnq_0/a_1772_2427# RSTn 0.00696f
C21 mux21_0/a_n2339_2762# VDD 0.07278f
C22 m2_n1268_1517# m2_n2888_1381# 0.32309f
C23 dffrnq_0/a_107_2787# RSTn 0
C24 dffsnq_0/a_6315_3300# dffrnq_0/a_1355_2471# 0
C25 m2_n1268_1517# m2_n1118_2715# 0.01606f
C26 VDD CLK 0.07919f
C27 MODE m2_n2888_1381# 0.03114f
C28 m2_n1118_2715# MODE 0.00199f
C29 REC_EN TREAT_EN 0.96508f
C30 dffsnq_0/a_4226_2960# dffrnq_0/a_n445_2787# 0
C31 REC_EN mux21_0/a_n2807_3163# 0
C32 m1_n1940_2465# REC_EN 0.04809f
C33 dffsnq_0/a_4022_2960# m2_n2888_1381# 0.01245f
C34 dffrnq_0/a_1772_2427# REC_EN 0.06518f
C35 dffsnq_0/a_4022_2960# m2_n1118_2715# 0.0012f
C36 REC_EN dffrnq_0/a_107_2787# 0.04683f
C37 dffsnq_0/a_5411_3360# dffrnq_0/a_1355_2471# 0.00389f
C38 m2_n1268_1517# dffsnq_0/a_4539_3312# 0.00178f
C39 dffrnq_0/a_n445_2787# dffrnq_0/a_n97_2787# -0
C40 m1_n1940_2465# TREAT_EN 0.09288f
C41 TREAT_EN mux21_0/a_n2807_3163# 0.0216f
C42 m1_n1940_2465# mux21_0/a_n2807_3163# 0.00362f
C43 mux21_0/a_n2035_3346# REC_EN 0
C44 dffrnq_0/a_n857_2466# m2_n2888_1381# 0.00435f
C45 TREAT_EN dffrnq_0/a_107_2787# 0
C46 dffrnq_0/a_n857_2466# m2_n1118_2715# 0.09109f
C47 CLK dffrnq_0/a_n445_2787# 0.00219f
C48 dffrnq_0/a_563_2471# RSTn 0
C49 m2_n1268_1517# VDD 0.07483f
C50 mux21_0/a_n2035_3346# TREAT_EN 0
C51 m2_n2888_1381# dffsnq_0/a_4479_2960# 0.00107f
C52 VDD MODE 0.02431f
C53 dffsnq_0/a_3222_3356# CLK 0.04043f
C54 dffrnq_0/a_395_2471# m2_n2888_1381# 0
C55 REC_EN nor2_1_0/a_n4929_4170# 0.00277f
C56 RSTn m2_n2888_1381# 0.08042f
C57 dffsnq_0/a_4539_3312# dffrnq_0/a_n857_2466# 0
C58 dffsnq_0/a_4022_2960# VDD -0
C59 m2_n1118_2715# RSTn 0
C60 dffrnq_0/a_563_2471# REC_EN 0
C61 dffrnq_0/a_415_2738# m2_n2888_1381# 0.00326f
C62 m2_n1118_2715# dffrnq_0/a_415_2738# 0.00111f
C63 TREAT_EN mux21_0/a_n2427_3346# 0
C64 TREAT_EN nor2_1_0/a_n4929_4170# 0.00385f
C65 REC_EN m2_n2888_1381# 0.09711f
C66 REC_EN m2_n1118_2715# 0.40328f
C67 VDD dffrnq_0/a_n857_2466# 0.00327f
C68 dffsnq_0/a_4539_3312# RSTn 0.00173f
C69 dffsnq_0/a_3634_2943# CLK 0.00346f
C70 REC_EN dffrnq_0/a_311_2787# 0.04302f
C71 dffsnq_0/a_4539_3312# dffrnq_0/a_415_2738# 0
C72 TREAT_EN m2_n2888_1381# 0.76438f
C73 dffsnq_0/a_6267_3356# RSTn 0.00141f
C74 m2_n2888_1381# mux21_0/a_n2807_3163# 0.06446f
C75 m1_n1940_2465# m2_n2888_1381# 0.0018f
C76 TREAT_EN m2_n1118_2715# 0.08524f
C77 dffrnq_0/a_1772_2427# m2_n2888_1381# 0.00389f
C78 m2_n1268_1517# dffsnq_0/a_3222_3356# 0.17173f
C79 m2_n1118_2715# mux21_0/a_n2807_3163# 0
C80 m1_n1940_2465# m2_n1118_2715# 0.00596f
C81 dffrnq_0/a_107_2787# m2_n2888_1381# 0.00276f
C82 dffsnq_0/a_4539_3312# REC_EN 0.00381f
C83 dffsnq_0/a_3222_3356# MODE 0
C84 dffsnq_0/a_5635_3360# RSTn 0.01481f
C85 VDD RSTn 0.01788f
C86 dffrnq_0/a_107_2787# m2_n1118_2715# 0.00379f
C87 dffsnq_0/a_4470_3360# REC_EN 0
C88 dffsnq_0/a_4226_2960# CLK 0
C89 VDD dffrnq_0/a_415_2738# 0
C90 REC_EN dffsnq_0/a_6267_3356# 0
C91 REC_EN nor2_2_0/a_n3725_1897# 0.00736f
C92 CLK dffrnq_0/a_n97_2787# 0
C93 REC_EN VDD 1.02684f
C94 dffsnq_0/a_5635_3360# REC_EN 0.00185f
C95 dffsnq_0/a_4539_3312# dffrnq_0/a_107_2787# 0
C96 TREAT_EN nor2_2_0/a_n3725_1897# 0.00212f
C97 m2_n1268_1517# dffsnq_0/a_3634_2943# 0.04806f
C98 mux21_0/a_n2339_2762# CLK 0
C99 dffsnq_0/a_3222_3356# dffrnq_0/a_n857_2466# 0.02445f
C100 dffrnq_0/a_1667_2471# RSTn 0.00326f
C101 dffrnq_0/a_n445_2787# RSTn 0.00218f
C102 VDD TREAT_EN 0.13379f
C103 m2_n2888_1381# nor2_1_0/a_n4929_4170# 0
C104 VDD mux21_0/a_n2807_3163# 0.00651f
C105 m1_n1940_2465# VDD 0.10995f
C106 dffsnq_0/a_3634_2943# dffsnq_0/a_4022_2960# -0
C107 dffrnq_0/a_1772_2427# VDD -0.00474f
C108 dffrnq_0/a_563_2471# m2_n2888_1381# 0
C109 VDD dffrnq_0/a_107_2787# 0
C110 m2_n1268_1517# dffsnq_0/a_4226_2960# 0.00325f
C111 dffsnq_0/a_3222_3356# RSTn 0.0017f
C112 REC_EN dffrnq_0/a_1667_2471# 0.01442f
C113 REC_EN dffrnq_0/a_n445_2787# 0.08524f
C114 dffsnq_0/a_3222_3356# dffrnq_0/a_415_2738# 0
C115 dffsnq_0/a_3634_2943# dffrnq_0/a_n857_2466# 0.00688f
C116 m2_n1118_2715# m2_n2888_1381# 0.01213f
C117 RSTn dffrnq_0/a_1355_2471# 0.00379f
C118 dffsnq_0/a_6315_3300# RSTn 0.04409f
C119 dffrnq_0/a_311_2787# m2_n2888_1381# 0
C120 mux21_0/a_n2339_2762# m2_n1268_1517# 0
C121 m2_n1118_2715# dffrnq_0/a_311_2787# 0.00134f
C122 REC_EN dffsnq_0/a_3222_3356# 0.00337f
C123 TREAT_EN dffrnq_0/a_n445_2787# 0
C124 mux21_0/a_n2339_2762# MODE 0.03694f
C125 m2_n1268_1517# CLK 0.15857f
C126 CLK MODE 0.04686f
C127 dffsnq_0/a_4226_2960# dffrnq_0/a_n857_2466# 0.00102f
C128 REC_EN dffrnq_0/a_1355_2471# 0.12679f
C129 dffsnq_0/a_4539_3312# m2_n2888_1381# 0.04591f
C130 dffsnq_0/a_3634_2943# RSTn 0.03997f
C131 VDD nor2_1_0/a_n4929_4170# 0
C132 RSTn dffsnq_0/a_4883_3360# 0
C133 dffsnq_0/a_4470_3360# m2_n2888_1381# 0
C134 REC_EN dffsnq_0/a_6315_3300# 0.00366f
C135 dffsnq_0/a_3222_3356# TREAT_EN 0.00124f
C136 dffsnq_0/a_4022_2960# CLK 0
C137 dffsnq_0/a_3634_2943# dffrnq_0/a_415_2738# 0
C138 dffsnq_0/a_3222_3356# mux21_0/a_n2807_3163# 0.00223f
C139 dffsnq_0/a_5411_3360# RSTn 0.054f
C140 m2_n1118_2715# nor2_2_0/a_n3725_1897# 0
C141 dffsnq_0/a_3634_2943# REC_EN 0.00662f
C142 dffsnq_0/a_5635_3360# m2_n2888_1381# 0.03634f
C143 VDD m2_n2888_1381# 0.97305f
C144 dffsnq_0/a_4226_2960# RSTn 0.00118f
C145 REC_EN dffsnq_0/a_4883_3360# 0
C146 VDD m2_n1118_2715# 0.07996f
C147 CLK dffrnq_0/a_n857_2466# 0.01924f
C148 dffrnq_0/a_1772_2427# dffsnq_0/a_6315_3300# 0.00394f
C149 dffsnq_0/a_4226_2960# dffrnq_0/a_415_2738# 0.00357f
C150 REC_EN dffsnq_0/a_5411_3360# 0.00463f
C151 dffsnq_0/a_3634_2943# TREAT_EN 0
C152 m2_n1268_1517# MODE 0.00203f
C153 REC_EN dffsnq_0/a_4226_2960# 0.00294f
C154 dffsnq_0/a_4539_3312# VDD -0
C155 m2_n1268_1517# dffsnq_0/a_4022_2960# 0.00534f
C156 dffrnq_0/a_395_2471# CLK 0
C157 dffrnq_0/a_1772_2427# dffsnq_0/a_5411_3360# 0
C158 dffrnq_0/a_2148_2471# RSTn 0
C159 CLK dffrnq_0/a_415_2738# 0
C160 dffrnq_0/a_1667_2471# m2_n2888_1381# 0
C161 dffrnq_0/a_n445_2787# m2_n2888_1381# 0.0061f
C162 REC_EN dffrnq_0/a_n97_2787# 0.0092f
C163 dffsnq_0/a_4226_2960# TREAT_EN 0
C164 VDD nor2_2_0/a_n3725_1897# 0
C165 dffrnq_0/a_n445_2787# m2_n1118_2715# 0.05126f
C166 mux21_0/a_n2339_2762# REC_EN 0.08079f
C167 dffsnq_0/a_4226_2960# dffrnq_0/a_107_2787# 0
C168 m2_n1268_1517# dffrnq_0/a_n857_2466# 0.00201f
C169 dffsnq_0/a_5635_3360# VDD -0
C170 REC_EN CLK 0.0199f
C171 REC_EN dffrnq_0/a_2148_2471# 0
C172 dffrnq_0/a_n857_2466# MODE 0
C173 dffsnq_0/a_3222_3356# m2_n2888_1381# 0.1587f
C174 TREAT_EN dffrnq_0/a_n97_2787# 0
C175 dffsnq_0/a_3222_3356# m2_n1118_2715# 0.00251f
C176 mux21_0/a_n2394_2806# TREAT_EN 0
C177 mux21_0/a_n2339_2762# TREAT_EN 0.07597f
C178 dffrnq_0/a_1355_2471# m2_n2888_1381# 0.00331f
C179 mux21_0/a_n2339_2762# mux21_0/a_n2807_3163# -0.00283f
C180 mux21_0/a_n2339_2762# m1_n1940_2465# 0
C181 dffsnq_0/a_4539_3312# dffrnq_0/a_n445_2787# 0.00273f
C182 m2_n1268_1517# dffsnq_0/a_4479_2960# 0
C183 TREAT_EN CLK 0.09284f
C184 CLK mux21_0/a_n2807_3163# 0.02062f
C185 dffsnq_0/a_6315_3300# m2_n2888_1381# 0.05467f
C186 m1_n1940_2465# CLK 0.00795f
C187 m2_n1268_1517# RSTn 0
C188 CLK dffrnq_0/a_107_2787# 0
C189 VDD dffrnq_0/a_n445_2787# 0
C190 dffsnq_0/a_3634_2943# m2_n2888_1381# 0.08736f
C191 m2_n2888_1381# dffsnq_0/a_4883_3360# 0
C192 dffsnq_0/a_3634_2943# m2_n1118_2715# 0
C193 m2_n1268_1517# REC_EN 0
C194 dffsnq_0/a_5411_3360# m2_n2888_1381# 0.03285f
C195 TREAT_EN mux21_0/a_n2035_2806# 0
C196 REC_EN MODE 0.13488f
C197 dffsnq_0/a_3222_3356# VDD 0.00338f
C198 dffsnq_0/a_4226_2960# m2_n2888_1381# 0.02954f
C199 dffsnq_0/a_4022_2960# REC_EN 0
C200 dffrnq_0/a_n857_2466# RSTn 0.00121f
C201 CLK mux21_0/a_n2427_3346# 0
C202 m2_n1268_1517# TREAT_EN 0.01613f
C203 VDD dffrnq_0/a_1355_2471# 0.00105f
C204 m2_n1268_1517# mux21_0/a_n2807_3163# 0.00266f
C205 TREAT_EN MODE 0.28553f
C206 MODE mux21_0/a_n2807_3163# 0.09448f
C207 dffsnq_0/a_5635_3360# dffsnq_0/a_6315_3300# -0
C208 dffsnq_0/a_6315_3300# VDD 0.00615f
C209 m1_n1940_2465# MODE 0.03848f
C210 dffsnq_0/a_4226_2960# dffrnq_0/a_311_2787# 0
C211 dffrnq_0/a_n97_2787# m2_n2888_1381# 0
C212 dffsnq_0/a_4022_2960# TREAT_EN 0
C213 m2_n1118_2715# dffrnq_0/a_n97_2787# 0.00551f
C214 REC_EN dffrnq_0/a_n857_2466# 0.0471f
C215 mux21_0/a_n2394_2806# m2_n2888_1381# 0.00103f
C216 mux21_0/a_n2339_2762# m2_n2888_1381# 0.03841f
C217 dffrnq_0/a_395_2471# RSTn 0
C218 dffsnq_0/a_3634_2943# VDD -0
C219 CLK m2_n2888_1381# 0.00687f
C220 m2_n2888_1381# VSS 1.35852f
C221 m2_n1118_2715# VSS 0.32666f
C222 REC_EN VSS 1.5599f
C223 RSTn VSS 2.34515f
C224 MODE VSS 1.15652f
C225 m1_n1940_2465# VSS 0.49336f
C226 TREAT_EN VSS 0.89223f
C227 nor2_1_0/a_n4929_4170# VSS -0
C228 VDD VSS 22.23366f
C229 dffrnq_0/a_1667_2471# VSS 0.01697f
C230 dffrnq_0/a_1772_2427# VSS 0.62774f
C231 dffrnq_0/a_1355_2471# VSS 0.37514f
C232 dffrnq_0/a_311_2787# VSS 0.01297f
C233 dffrnq_0/a_107_2787# VSS 0.29173f
C234 dffrnq_0/a_n97_2787# VSS 0.02321f
C235 dffrnq_0/a_415_2738# VSS 0.28147f
C236 dffrnq_0/a_n445_2787# VSS 0.68798f
C237 dffrnq_0/a_n857_2466# VSS 1.46629f
C238 CLK VSS 0.86461f
C239 mux21_0/a_n2339_2762# VSS 0.46031f
C240 mux21_0/a_n2807_3163# VSS 0.32921f
C241 m2_n1268_1517# VSS 0.34757f
C242 dffsnq_0/a_6315_3300# VSS 0.58924f
C243 dffsnq_0/a_5635_3360# VSS 0.04999f
C244 dffsnq_0/a_5411_3360# VSS 0.43599f
C245 dffsnq_0/a_4022_2960# VSS 0.01977f
C246 dffsnq_0/a_4226_2960# VSS 0.3038f
C247 dffsnq_0/a_4539_3312# VSS 0.28789f
C248 dffsnq_0/a_3634_2943# VSS 1.22248f
C249 dffsnq_0/a_3222_3356# VSS 1.32709f
.ends

X1 MODE RSTn vss CLK vdd TREAT_EN REC_EN FSM





.control
save all
**
** ---- clock ----
let fclk     = 1e5
let tper_clk = 1/fclk
let tfr_clk  = 0.01*tper_clk
let ton_clk  = 0.5*tper_clk - 2*tfr_clk
let tper2clk = 0.95*tper_clk
**
** ---- resolution follows the fastest edge in the deck ----
let tmax  = tfr_clk/200
let tstep = tmax
**
** ---- 24 clock periods is enough to walk every transition ----
let tstop = 24*tper_clk
**
** ---- MODE: square wave, 8 clock periods per half ----
let tfr    = tfr_clk
let tper_D = 16*tper_clk
let ton_D  = 0.5*tper_D - 2*tfr
**
** ---- RSTn: low for the first 2 clock periods, then high ----
let td_R = 2*tper_clk
**
alter @v4[PULSE] = [ 0 3.3 0 $&tfr_clk $&tfr_clk $&ton_clk $&tper2clk 0 ]
alter @v3[PULSE] = [ 0 3.3 0 $&tfr $&tfr $&ton_D $&tper_D 0 ]
alter @v5[PULSE] = [ 0 3.3 $&td_R $&tfr $&tfr $&tstop $&tstop 0 ]
**
op
tran $&tstep $&tstop 0 $&tmax
**
plot v(clk) v(mode)+5 v(rstn)+10 v(rec_en)+15 v(treat_en)+20
write fsm_fast.raw
.endc





**** end user architecture code
**.ends
.GLOBAL GND
.end
